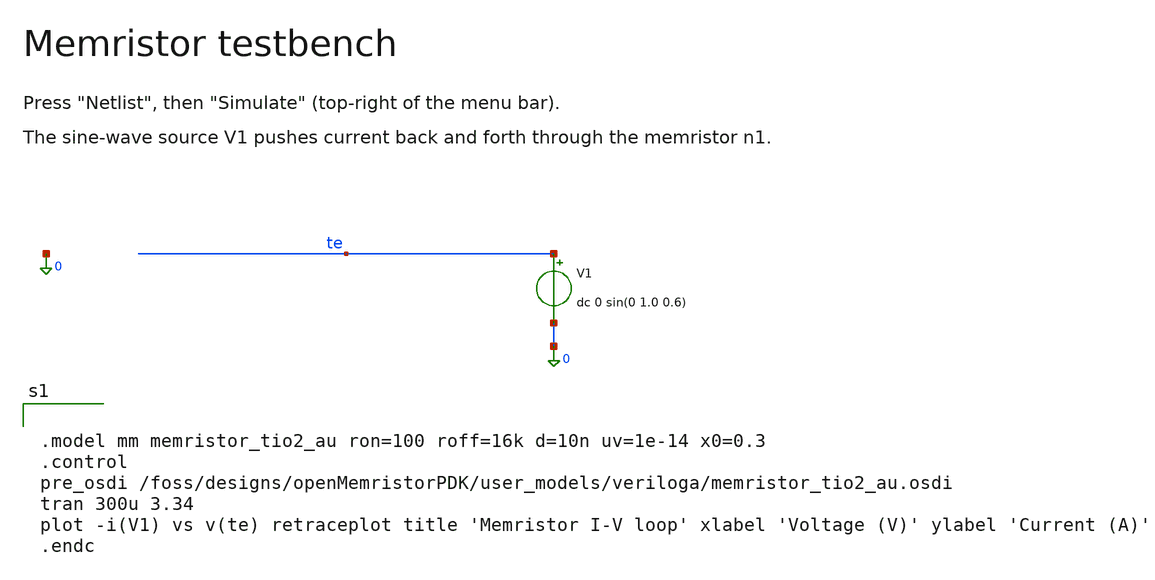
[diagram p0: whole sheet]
** sch_path: libraries/openmemristorpdk_pr/memristor_tio2_au_tb.sch
**.subckt memristor_tio2_au_tb
V1 te 0 dc 0 sin(0 1.0 0.6)
**** begin user architecture code


.model mm memristor_tio2_au ron=100 roff=16k d=10n uv=1e-14 x0=0.3
.control
pre_osdi /foss/designs/openMemristorPDK/user_models/veriloga/memristor_tio2_au.osdi
tran 300u 3.34
plot -i(V1) vs v(te) retraceplot title 'Memristor I-V loop' xlabel 'Voltage (V)' ylabel 'Current (A)'
.endc


**** end user architecture code
**.ends
.end
